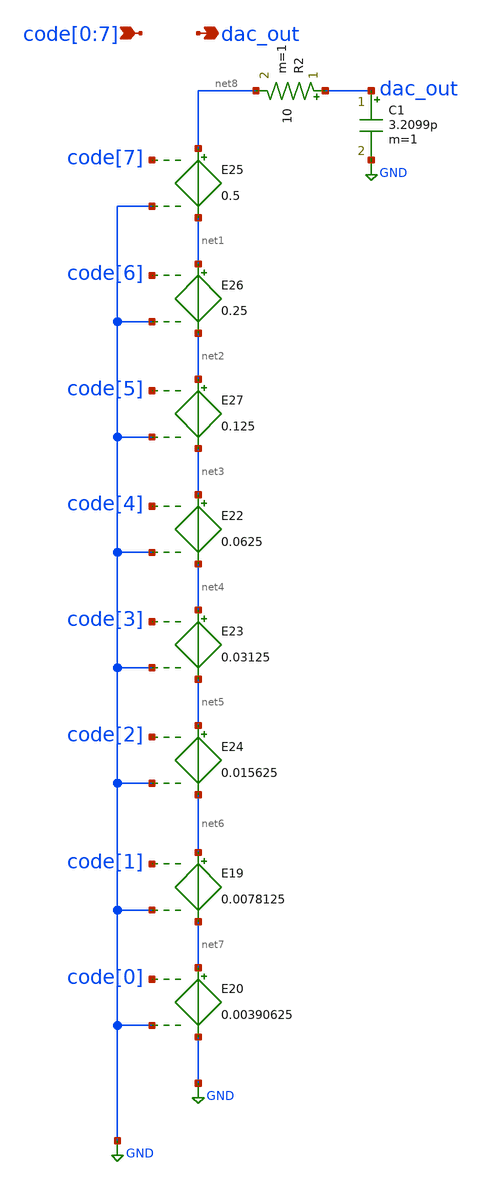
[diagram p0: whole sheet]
** sch_path: xschem/ideal_dac.sch
**.subckt ideal_dac code[0],code[1],code[2],code[3],code[4],code[5],code[6],code[7] dac_out
*.ipin code[0],code[1],code[2],code[3],code[4],code[5],code[6],code[7]
*.opin dac_out
E19 net6 net7 code[1] GND 0.0078125
E20 net7 GND code[0] GND 0.00390625
E22 net3 net4 code[4] GND 0.0625
E23 net4 net5 code[3] GND 0.03125
E24 net5 net6 code[2] GND 0.015625
E25 net8 net1 code[7] GND 0.5
E26 net1 net2 code[6] GND 0.25
E27 net2 net3 code[5] GND 0.125
R2 dac_out net8 10 m=1
C1 dac_out GND 3.2099p m=1
**.ends
.GLOBAL GND
.end
